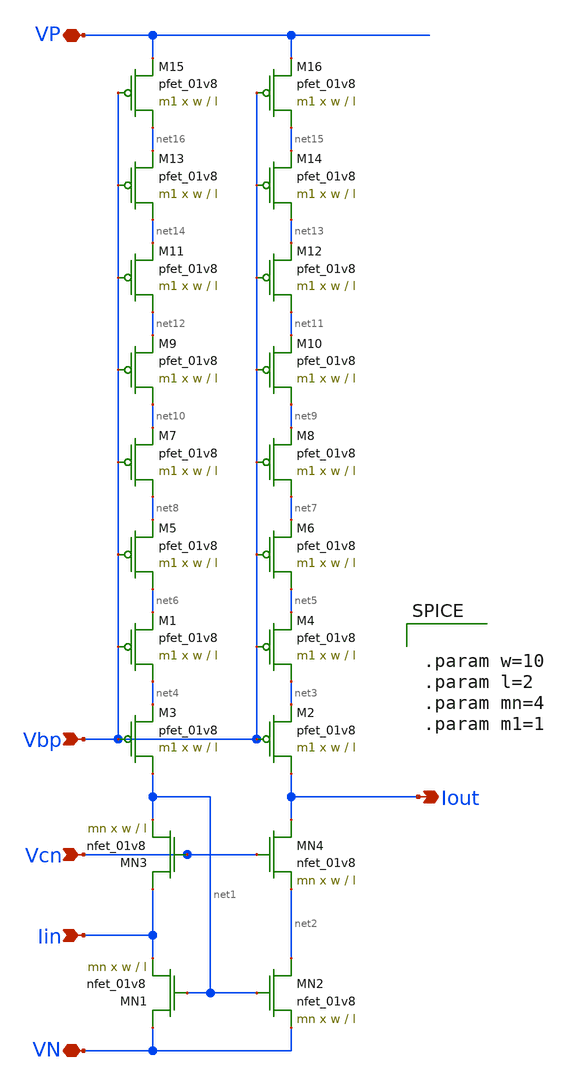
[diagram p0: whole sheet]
** sch_path: iout_mirror.sch
**.subckt iout_mirror Vbp VN Iout Iin Vcn VP
*.ipin Vbp
*.iopin VN
*.opin Iout
*.ipin Iin
*.ipin Vcn
*.iopin VP
XM3 net1 Vbp net4 VDD sky130_fd_pr__pfet_01v8 L=l W=w nf=1 ad='int((nf+1)/2) * W/nf * 0.29' as='int((nf+2)/2) * W/nf * 0.29'
+ pd='2*int((nf+1)/2) * (W/nf + 0.29)' ps='2*int((nf+2)/2) * (W/nf + 0.29)' nrd='0.29 / W' nrs='0.29 / W'
+ sa=0 sb=0 sd=0 mult=m1 m=m1
XM2 Iout Vbp net3 VDD sky130_fd_pr__pfet_01v8 L=l W=w nf=1 ad='int((nf+1)/2) * W/nf * 0.29' as='int((nf+2)/2) * W/nf * 0.29'
+ pd='2*int((nf+1)/2) * (W/nf + 0.29)' ps='2*int((nf+2)/2) * (W/nf + 0.29)' nrd='0.29 / W' nrs='0.29 / W'
+ sa=0 sb=0 sd=0 mult=m1 m=m1
XMN1 VN net1 Iin GND sky130_fd_pr__nfet_01v8 L=l W=w nf=1 ad='int((nf+1)/2) * W/nf * 0.29' as='int((nf+2)/2) * W/nf * 0.29'
+ pd='2*int((nf+1)/2) * (W/nf + 0.29)' ps='2*int((nf+2)/2) * (W/nf + 0.29)' nrd='0.29 / W' nrs='0.29 / W'
+ sa=0 sb=0 sd=0 mult=mn m=mn
XMN2 net2 net1 VN GND sky130_fd_pr__nfet_01v8 L=l W=w nf=1 ad='int((nf+1)/2) * W/nf * 0.29' as='int((nf+2)/2) * W/nf * 0.29'
+ pd='2*int((nf+1)/2) * (W/nf + 0.29)' ps='2*int((nf+2)/2) * (W/nf + 0.29)' nrd='0.29 / W' nrs='0.29 / W'
+ sa=0 sb=0 sd=0 mult=mn m=mn
XMN3 Iin Vcn net1 GND sky130_fd_pr__nfet_01v8 L=l W=w nf=1 ad='int((nf+1)/2) * W/nf * 0.29' as='int((nf+2)/2) * W/nf * 0.29'
+ pd='2*int((nf+1)/2) * (W/nf + 0.29)' ps='2*int((nf+2)/2) * (W/nf + 0.29)' nrd='0.29 / W' nrs='0.29 / W'
+ sa=0 sb=0 sd=0 mult=mn m=mn
XMN4 Iout Vcn net2 GND sky130_fd_pr__nfet_01v8 L=l W=w nf=1 ad='int((nf+1)/2) * W/nf * 0.29' as='int((nf+2)/2) * W/nf * 0.29'
+ pd='2*int((nf+1)/2) * (W/nf + 0.29)' ps='2*int((nf+2)/2) * (W/nf + 0.29)' nrd='0.29 / W' nrs='0.29 / W'
+ sa=0 sb=0 sd=0 mult=mn m=mn
XM1 net4 Vbp net6 VDD sky130_fd_pr__pfet_01v8 L=l W=w nf=1 ad='int((nf+1)/2) * W/nf * 0.29' as='int((nf+2)/2) * W/nf * 0.29'
+ pd='2*int((nf+1)/2) * (W/nf + 0.29)' ps='2*int((nf+2)/2) * (W/nf + 0.29)' nrd='0.29 / W' nrs='0.29 / W'
+ sa=0 sb=0 sd=0 mult=m1 m=m1
XM4 net3 Vbp net5 VDD sky130_fd_pr__pfet_01v8 L=l W=w nf=1 ad='int((nf+1)/2) * W/nf * 0.29' as='int((nf+2)/2) * W/nf * 0.29'
+ pd='2*int((nf+1)/2) * (W/nf + 0.29)' ps='2*int((nf+2)/2) * (W/nf + 0.29)' nrd='0.29 / W' nrs='0.29 / W'
+ sa=0 sb=0 sd=0 mult=m1 m=m1
XM5 net6 Vbp net8 VDD sky130_fd_pr__pfet_01v8 L=l W=w nf=1 ad='int((nf+1)/2) * W/nf * 0.29' as='int((nf+2)/2) * W/nf * 0.29'
+ pd='2*int((nf+1)/2) * (W/nf + 0.29)' ps='2*int((nf+2)/2) * (W/nf + 0.29)' nrd='0.29 / W' nrs='0.29 / W'
+ sa=0 sb=0 sd=0 mult=m1 m=m1
XM6 net5 Vbp net7 VDD sky130_fd_pr__pfet_01v8 L=l W=w nf=1 ad='int((nf+1)/2) * W/nf * 0.29' as='int((nf+2)/2) * W/nf * 0.29'
+ pd='2*int((nf+1)/2) * (W/nf + 0.29)' ps='2*int((nf+2)/2) * (W/nf + 0.29)' nrd='0.29 / W' nrs='0.29 / W'
+ sa=0 sb=0 sd=0 mult=m1 m=m1
XM7 net8 Vbp net10 VDD sky130_fd_pr__pfet_01v8 L=l W=w nf=1 ad='int((nf+1)/2) * W/nf * 0.29' as='int((nf+2)/2) * W/nf * 0.29'
+ pd='2*int((nf+1)/2) * (W/nf + 0.29)' ps='2*int((nf+2)/2) * (W/nf + 0.29)' nrd='0.29 / W' nrs='0.29 / W'
+ sa=0 sb=0 sd=0 mult=m1 m=m1
XM8 net7 Vbp net9 VDD sky130_fd_pr__pfet_01v8 L=l W=w nf=1 ad='int((nf+1)/2) * W/nf * 0.29' as='int((nf+2)/2) * W/nf * 0.29'
+ pd='2*int((nf+1)/2) * (W/nf + 0.29)' ps='2*int((nf+2)/2) * (W/nf + 0.29)' nrd='0.29 / W' nrs='0.29 / W'
+ sa=0 sb=0 sd=0 mult=m1 m=m1
XM9 net10 Vbp net12 VDD sky130_fd_pr__pfet_01v8 L=l W=w nf=1 ad='int((nf+1)/2) * W/nf * 0.29' as='int((nf+2)/2) * W/nf * 0.29'
+ pd='2*int((nf+1)/2) * (W/nf + 0.29)' ps='2*int((nf+2)/2) * (W/nf + 0.29)' nrd='0.29 / W' nrs='0.29 / W'
+ sa=0 sb=0 sd=0 mult=m1 m=m1
XM10 net9 Vbp net11 VDD sky130_fd_pr__pfet_01v8 L=l W=w nf=1 ad='int((nf+1)/2) * W/nf * 0.29' as='int((nf+2)/2) * W/nf * 0.29'
+ pd='2*int((nf+1)/2) * (W/nf + 0.29)' ps='2*int((nf+2)/2) * (W/nf + 0.29)' nrd='0.29 / W' nrs='0.29 / W'
+ sa=0 sb=0 sd=0 mult=m1 m=m1
XM11 net12 Vbp net14 VDD sky130_fd_pr__pfet_01v8 L=l W=w nf=1 ad='int((nf+1)/2) * W/nf * 0.29' as='int((nf+2)/2) * W/nf * 0.29'
+ pd='2*int((nf+1)/2) * (W/nf + 0.29)' ps='2*int((nf+2)/2) * (W/nf + 0.29)' nrd='0.29 / W' nrs='0.29 / W'
+ sa=0 sb=0 sd=0 mult=m1 m=m1
XM12 net11 Vbp net13 VDD sky130_fd_pr__pfet_01v8 L=l W=w nf=1 ad='int((nf+1)/2) * W/nf * 0.29' as='int((nf+2)/2) * W/nf * 0.29'
+ pd='2*int((nf+1)/2) * (W/nf + 0.29)' ps='2*int((nf+2)/2) * (W/nf + 0.29)' nrd='0.29 / W' nrs='0.29 / W'
+ sa=0 sb=0 sd=0 mult=m1 m=m1
XM13 net14 Vbp net16 VDD sky130_fd_pr__pfet_01v8 L=l W=w nf=1 ad='int((nf+1)/2) * W/nf * 0.29' as='int((nf+2)/2) * W/nf * 0.29'
+ pd='2*int((nf+1)/2) * (W/nf + 0.29)' ps='2*int((nf+2)/2) * (W/nf + 0.29)' nrd='0.29 / W' nrs='0.29 / W'
+ sa=0 sb=0 sd=0 mult=m1 m=m1
XM14 net13 Vbp net15 VDD sky130_fd_pr__pfet_01v8 L=l W=w nf=1 ad='int((nf+1)/2) * W/nf * 0.29' as='int((nf+2)/2) * W/nf * 0.29'
+ pd='2*int((nf+1)/2) * (W/nf + 0.29)' ps='2*int((nf+2)/2) * (W/nf + 0.29)' nrd='0.29 / W' nrs='0.29 / W'
+ sa=0 sb=0 sd=0 mult=m1 m=m1
XM15 net16 Vbp VP VDD sky130_fd_pr__pfet_01v8 L=l W=w nf=1 ad='int((nf+1)/2) * W/nf * 0.29' as='int((nf+2)/2) * W/nf * 0.29'
+ pd='2*int((nf+1)/2) * (W/nf + 0.29)' ps='2*int((nf+2)/2) * (W/nf + 0.29)' nrd='0.29 / W' nrs='0.29 / W'
+ sa=0 sb=0 sd=0 mult=m1 m=m1
XM16 net15 Vbp VP VDD sky130_fd_pr__pfet_01v8 L=l W=w nf=1 ad='int((nf+1)/2) * W/nf * 0.29' as='int((nf+2)/2) * W/nf * 0.29'
+ pd='2*int((nf+1)/2) * (W/nf + 0.29)' ps='2*int((nf+2)/2) * (W/nf + 0.29)' nrd='0.29 / W' nrs='0.29 / W'
+ sa=0 sb=0 sd=0 mult=m1 m=m1
**** begin user architecture code


.param w=10
.param l=2
.param mn=4
.param m1=1


**** end user architecture code
**.ends
.end
